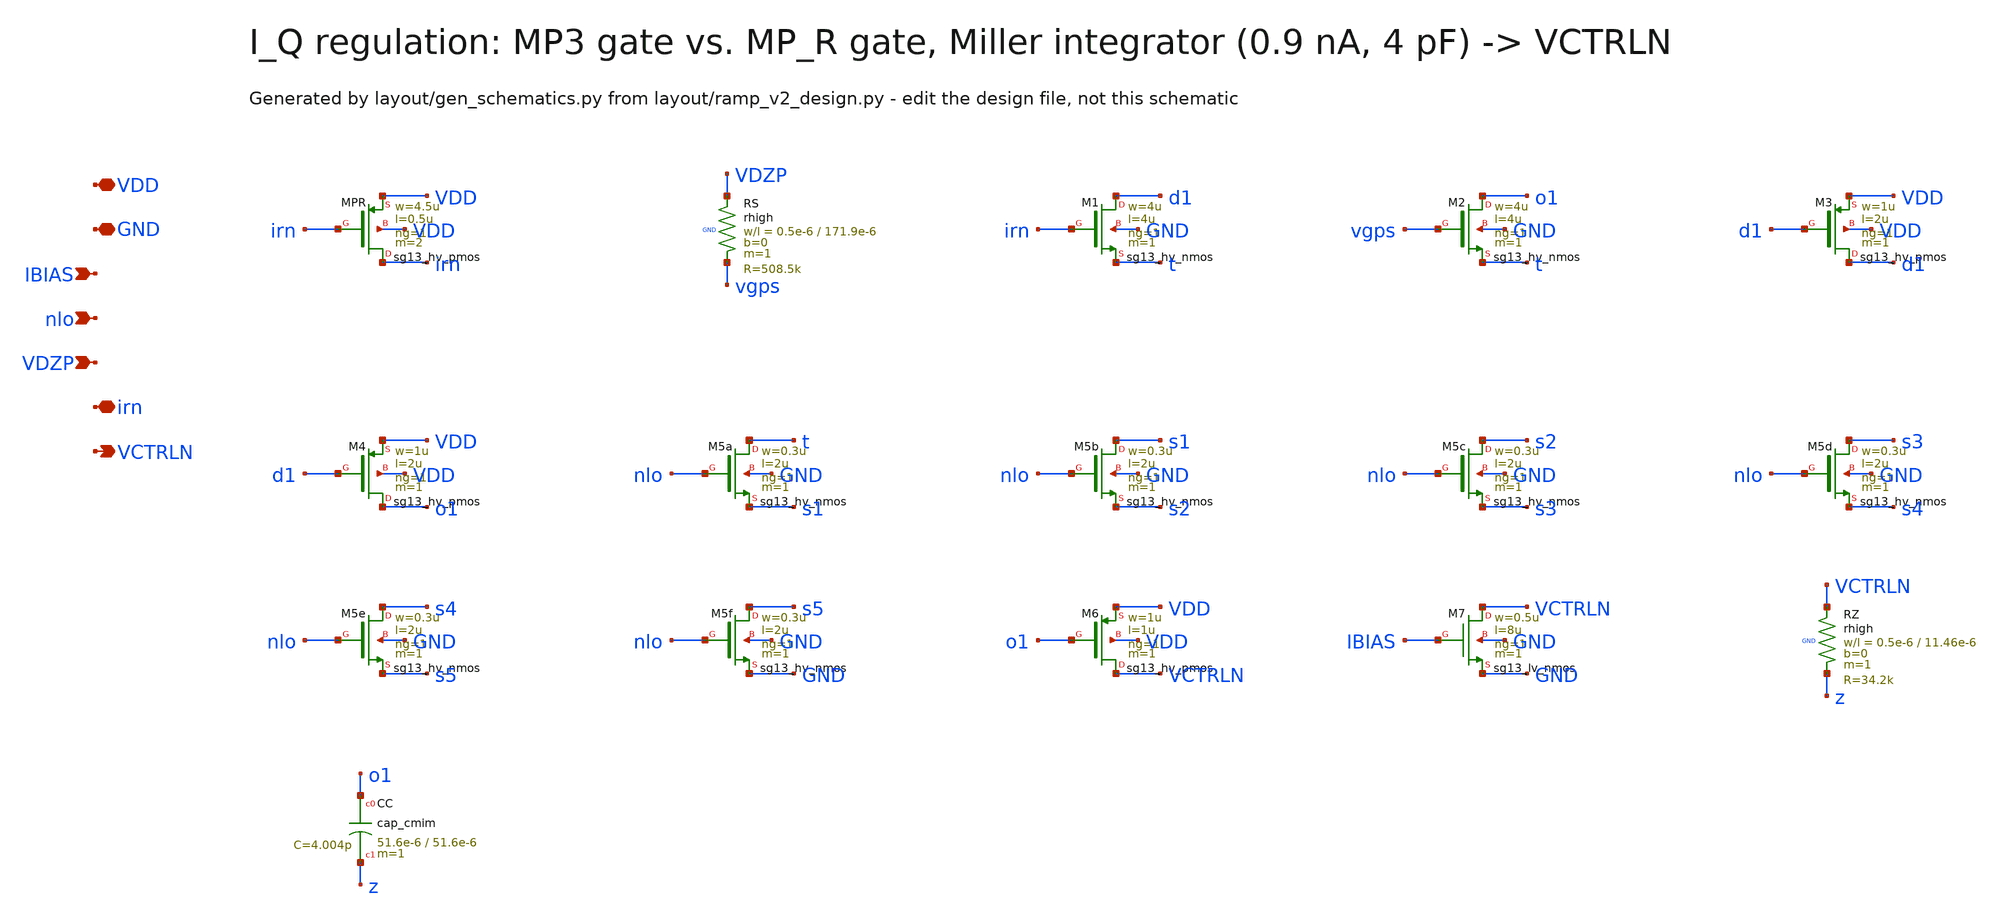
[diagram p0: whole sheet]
** sch_path: Design Files/RAMP/RAMP-V2/REG_V2.sch
**.subckt REG_V2 VDD GND IBIAS nlo VDZP irn VCTRLN
*.iopin VDD
*.iopin GND
*.ipin IBIAS
*.ipin nlo
*.ipin VDZP
*.iopin irn
*.opin VCTRLN
XMPR irn irn VDD VDD sg13_hv_pmos w=4.5u l=0.5u ng=1 m=2 mm_ok=1
XRS VDZP vgps GND rhigh w=0.5e-6 l=171.9e-6 m=1 b=0 mm_ok=1
XM1 d1 irn t GND sg13_hv_nmos w=4u l=4u ng=1 m=1 mm_ok=1
XM2 o1 vgps t GND sg13_hv_nmos w=4u l=4u ng=1 m=1 mm_ok=1
XM3 d1 d1 VDD VDD sg13_hv_pmos w=1u l=2u ng=1 m=1 mm_ok=1
XM4 o1 d1 VDD VDD sg13_hv_pmos w=1u l=2u ng=1 m=1 mm_ok=1
XM5a t nlo s1 GND sg13_hv_nmos w=0.3u l=2u ng=1 m=1 mm_ok=1
XM5b s1 nlo s2 GND sg13_hv_nmos w=0.3u l=2u ng=1 m=1 mm_ok=1
XM5c s2 nlo s3 GND sg13_hv_nmos w=0.3u l=2u ng=1 m=1 mm_ok=1
XM5d s3 nlo s4 GND sg13_hv_nmos w=0.3u l=2u ng=1 m=1 mm_ok=1
XM5e s4 nlo s5 GND sg13_hv_nmos w=0.3u l=2u ng=1 m=1 mm_ok=1
XM5f s5 nlo GND GND sg13_hv_nmos w=0.3u l=2u ng=1 m=1 mm_ok=1
XM6 VCTRLN o1 VDD VDD sg13_hv_pmos w=1u l=1u ng=1 m=1 mm_ok=1
XM7 VCTRLN IBIAS GND GND sg13_lv_nmos w=0.5u l=8u ng=1 m=1 mm_ok=1
XRZ VCTRLN z GND rhigh w=0.5e-6 l=11.46e-6 m=1 b=0 mm_ok=1
XCC o1 z cap_cmim w=51.6e-6 l=51.6e-6 m=1 mm_ok=1
**.ends
.end
